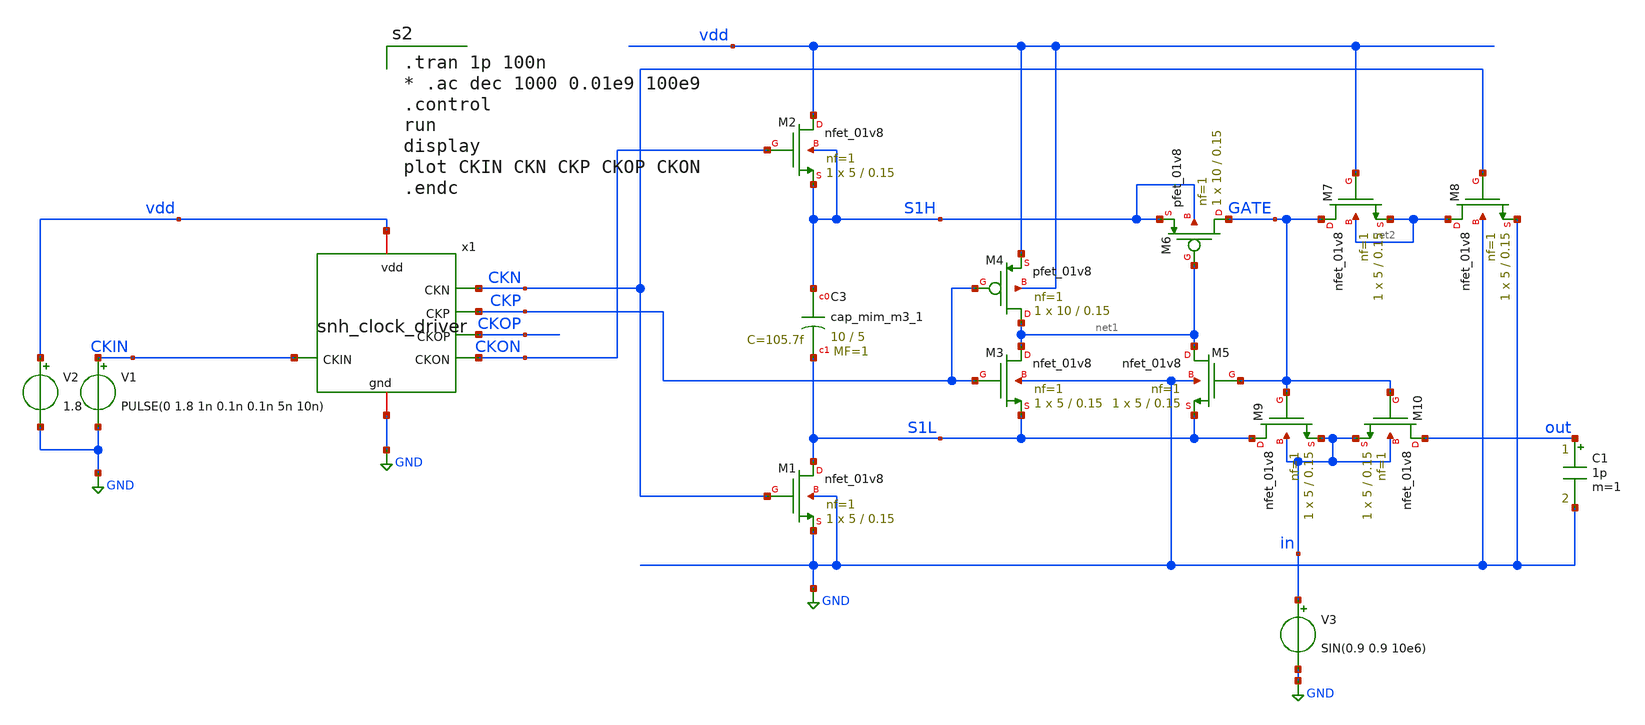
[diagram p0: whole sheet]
** sch_path: xschem/snh_clock_driver_test.sch
**.subckt snh_clock_driver_test
V1 CKIN GND PULSE(0 1.8 1n 0.1n 0.1n 5n 10n)
V2 vdd GND 1.8
x1 vdd CKN CKP CKOP CKON CKIN GND snh_clock_driver
XC3 S1H S1L sky130_fd_pr__cap_mim_m3_1 W=10 L=5 MF=1 m=1
XM2 vdd CKON S1H S1H sky130_fd_pr__nfet_01v8 L=0.15 W=5 nf=1 ad='int((nf+1)/2) * W/nf * 0.29' as='int((nf+2)/2) * W/nf * 0.29'
+ pd='2*int((nf+1)/2) * (W/nf + 0.29)' ps='2*int((nf+2)/2) * (W/nf + 0.29)' nrd='0.29 / W' nrs='0.29 / W'
+ sa=0 sb=0 sd=0 mult=1 m=1
XM1 S1L CKN GND GND sky130_fd_pr__nfet_01v8 L=0.15 W=5 nf=1 ad='int((nf+1)/2) * W/nf * 0.29' as='int((nf+2)/2) * W/nf * 0.29'
+ pd='2*int((nf+1)/2) * (W/nf + 0.29)' ps='2*int((nf+2)/2) * (W/nf + 0.29)' nrd='0.29 / W' nrs='0.29 / W'
+ sa=0 sb=0 sd=0 mult=1 m=1
XM3 net1 CKP S1L GND sky130_fd_pr__nfet_01v8 L=0.15 W=5 nf=1 ad='int((nf+1)/2) * W/nf * 0.29' as='int((nf+2)/2) * W/nf * 0.29'
+ pd='2*int((nf+1)/2) * (W/nf + 0.29)' ps='2*int((nf+2)/2) * (W/nf + 0.29)' nrd='0.29 / W' nrs='0.29 / W'
+ sa=0 sb=0 sd=0 mult=1 m=1
XM4 net1 CKP vdd vdd sky130_fd_pr__pfet_01v8 L=0.15 W=10 nf=1 ad='int((nf+1)/2) * W/nf * 0.29' as='int((nf+2)/2) * W/nf * 0.29'
+ pd='2*int((nf+1)/2) * (W/nf + 0.29)' ps='2*int((nf+2)/2) * (W/nf + 0.29)' nrd='0.29 / W' nrs='0.29 / W'
+ sa=0 sb=0 sd=0 mult=1 m=1
XM5 net1 GATE S1L GND sky130_fd_pr__nfet_01v8 L=0.15 W=5 nf=1 ad='int((nf+1)/2) * W/nf * 0.29' as='int((nf+2)/2) * W/nf * 0.29'
+ pd='2*int((nf+1)/2) * (W/nf + 0.29)' ps='2*int((nf+2)/2) * (W/nf + 0.29)' nrd='0.29 / W' nrs='0.29 / W'
+ sa=0 sb=0 sd=0 mult=1 m=1
XM6 GATE net1 S1H S1H sky130_fd_pr__pfet_01v8 L=0.15 W=10 nf=1 ad='int((nf+1)/2) * W/nf * 0.29' as='int((nf+2)/2) * W/nf * 0.29'
+ pd='2*int((nf+1)/2) * (W/nf + 0.29)' ps='2*int((nf+2)/2) * (W/nf + 0.29)' nrd='0.29 / W' nrs='0.29 / W'
+ sa=0 sb=0 sd=0 mult=1 m=1
XM7 GATE vdd net2 net2 sky130_fd_pr__nfet_01v8 L=0.15 W=5 nf=1 ad='int((nf+1)/2) * W/nf * 0.29' as='int((nf+2)/2) * W/nf * 0.29'
+ pd='2*int((nf+1)/2) * (W/nf + 0.29)' ps='2*int((nf+2)/2) * (W/nf + 0.29)' nrd='0.29 / W' nrs='0.29 / W'
+ sa=0 sb=0 sd=0 mult=1 m=1
XM8 net2 CKN GND GND sky130_fd_pr__nfet_01v8 L=0.15 W=5 nf=1 ad='int((nf+1)/2) * W/nf * 0.29' as='int((nf+2)/2) * W/nf * 0.29'
+ pd='2*int((nf+1)/2) * (W/nf + 0.29)' ps='2*int((nf+2)/2) * (W/nf + 0.29)' nrd='0.29 / W' nrs='0.29 / W'
+ sa=0 sb=0 sd=0 mult=1 m=1
XM9 S1L GATE in in sky130_fd_pr__nfet_01v8 L=0.15 W=5 nf=1 ad='int((nf+1)/2) * W/nf * 0.29' as='int((nf+2)/2) * W/nf * 0.29'
+ pd='2*int((nf+1)/2) * (W/nf + 0.29)' ps='2*int((nf+2)/2) * (W/nf + 0.29)' nrd='0.29 / W' nrs='0.29 / W'
+ sa=0 sb=0 sd=0 mult=1 m=1
XM10 out GATE in in sky130_fd_pr__nfet_01v8 L=0.15 W=5 nf=1 ad='int((nf+1)/2) * W/nf * 0.29' as='int((nf+2)/2) * W/nf * 0.29'
+ pd='2*int((nf+1)/2) * (W/nf + 0.29)' ps='2*int((nf+2)/2) * (W/nf + 0.29)' nrd='0.29 / W' nrs='0.29 / W'
+ sa=0 sb=0 sd=0 mult=1 m=1
C1 out GND 1p m=1
V3 in GND SIN(0.9 0.9 10e6)
**** begin user architecture code
.lib $::SKYWATER_MODELS/sky130.lib.spice tt
.include /home/al/openmpw/pdk_1/sky130B/libs.ref/sky130_fd_sc_hd/spice/sky130_fd_sc_hd.spice


.tran 1p 100n
* .ac dec 1000 0.01e9 100e9
.control
run
display
plot CKIN CKN CKP CKOP CKON
.endc


**** end user architecture code
**.ends

* expanding   symbol:  snh_clock_driver.sym # of pins=7
** sym_path: xschem/snh_clock_driver.sym
** sch_path: xschem/snh_clock_driver.sch
.subckt snh_clock_driver vdd CKN CKP CKOP CKON CKIN gnd
*.iopin vdd
*.iopin gnd
*.ipin CKIN
*.opin CKN
*.opin CKP
*.opin CKOP
*.opin CKON
XC1 CKON CKN sky130_fd_pr__cap_mim_m3_1 W=10 L=5 MF=1 m=1
XC3 CKOP CKP sky130_fd_pr__cap_mim_m3_1 W=10 L=5 MF=1 m=1
x3 CKBUF gnd gnd vdd vdd CKP sky130_fd_sc_hd__clkinv_8
x2 CKBUF gnd gnd vdd vdd CKN sky130_fd_sc_hd__clkbuf_8
x1 net1 gnd gnd vdd vdd CKBUF sky130_fd_sc_hd__clkbuf_8
XM2 vdd CKOP CKON gnd sky130_fd_pr__nfet_03v3_nvt L=0.5 W=1 nf=1 ad='int((nf+1)/2) * W/nf * 0.29' as='int((nf+2)/2) * W/nf * 0.29'
+ pd='2*int((nf+1)/2) * (W/nf + 0.29)' ps='2*int((nf+2)/2) * (W/nf + 0.29)' nrd='0.29 / W' nrs='0.29 / W'
+ sa=0 sb=0 sd=0 mult=5 m=5
x4 CKBUF gnd gnd vdd vdd CKP sky130_fd_sc_hd__clkinv_8
x5 CKBUF gnd gnd vdd vdd CKN sky130_fd_sc_hd__clkbuf_8
x6 CKIN gnd gnd vdd vdd net1 sky130_fd_sc_hd__clkbuf_2
XM1 vdd CKON CKOP gnd sky130_fd_pr__nfet_03v3_nvt L=0.5 W=1 nf=1 ad='int((nf+1)/2) * W/nf * 0.29' as='int((nf+2)/2) * W/nf * 0.29'
+ pd='2*int((nf+1)/2) * (W/nf + 0.29)' ps='2*int((nf+2)/2) * (W/nf + 0.29)' nrd='0.29 / W' nrs='0.29 / W'
+ sa=0 sb=0 sd=0 mult=5 m=5
.ends

.GLOBAL GND
.end
